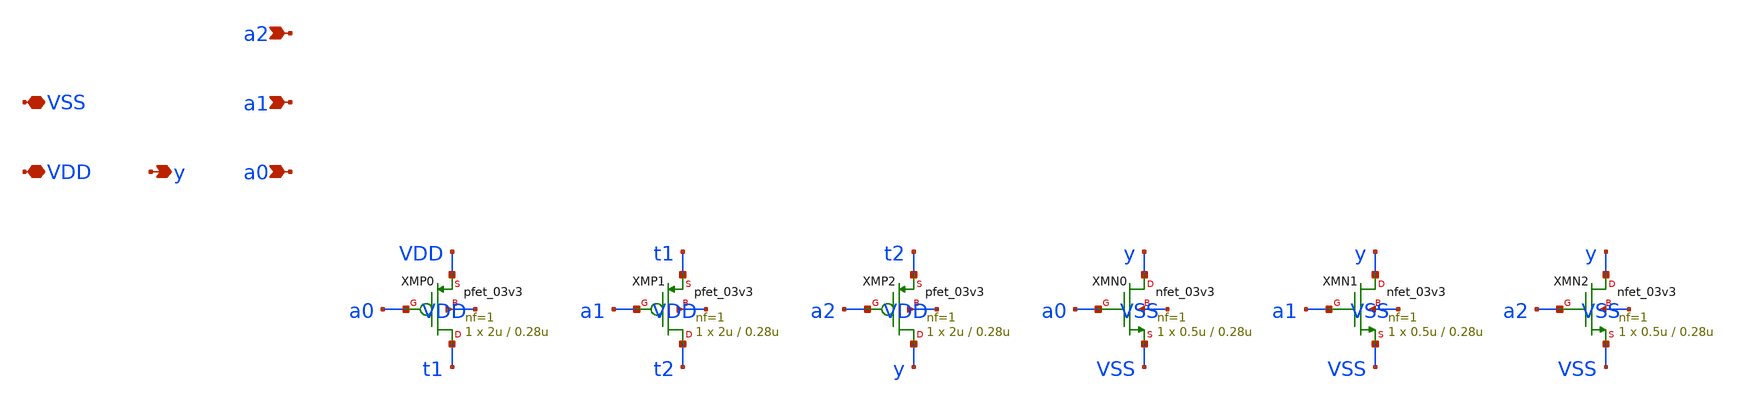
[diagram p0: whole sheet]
** sch_path: design/nor3.sch
**.subckt nor3 a0 a1 a2 y VDD VSS
*.ipin a0
*.ipin a1
*.ipin a2
*.opin y
*.iopin VDD
*.iopin VSS
XMP0 t1 a0 VDD VDD pfet_03v3 L=0.28u W=2u nf=1 ad='int((nf+1)/2) * W/nf * 0.18u' as='int((nf+2)/2) * W/nf * 0.18u'
+ pd='2*int((nf+1)/2) * (W/nf + 0.18u)' ps='2*int((nf+2)/2) * (W/nf + 0.18u)' nrd='0.18u / W' nrs='0.18u / W'
+ sa=0 sb=0 sd=0 m=1
XMP1 t2 a1 t1 VDD pfet_03v3 L=0.28u W=2u nf=1 ad='int((nf+1)/2) * W/nf * 0.18u' as='int((nf+2)/2) * W/nf * 0.18u'
+ pd='2*int((nf+1)/2) * (W/nf + 0.18u)' ps='2*int((nf+2)/2) * (W/nf + 0.18u)' nrd='0.18u / W' nrs='0.18u / W'
+ sa=0 sb=0 sd=0 m=1
XMP2 y a2 t2 VDD pfet_03v3 L=0.28u W=2u nf=1 ad='int((nf+1)/2) * W/nf * 0.18u' as='int((nf+2)/2) * W/nf * 0.18u'
+ pd='2*int((nf+1)/2) * (W/nf + 0.18u)' ps='2*int((nf+2)/2) * (W/nf + 0.18u)' nrd='0.18u / W' nrs='0.18u / W'
+ sa=0 sb=0 sd=0 m=1
XMN0 y a0 VSS VSS nfet_03v3 L=0.28u W=0.5u nf=1 ad='int((nf+1)/2) * W/nf * 0.18u' as='int((nf+2)/2) * W/nf * 0.18u'
+ pd='2*int((nf+1)/2) * (W/nf + 0.18u)' ps='2*int((nf+2)/2) * (W/nf + 0.18u)' nrd='0.18u / W' nrs='0.18u / W'
+ sa=0 sb=0 sd=0 m=1
XMN1 y a1 VSS VSS nfet_03v3 L=0.28u W=0.5u nf=1 ad='int((nf+1)/2) * W/nf * 0.18u' as='int((nf+2)/2) * W/nf * 0.18u'
+ pd='2*int((nf+1)/2) * (W/nf + 0.18u)' ps='2*int((nf+2)/2) * (W/nf + 0.18u)' nrd='0.18u / W' nrs='0.18u / W'
+ sa=0 sb=0 sd=0 m=1
XMN2 y a2 VSS VSS nfet_03v3 L=0.28u W=0.5u nf=1 ad='int((nf+1)/2) * W/nf * 0.18u' as='int((nf+2)/2) * W/nf * 0.18u'
+ pd='2*int((nf+1)/2) * (W/nf + 0.18u)' ps='2*int((nf+2)/2) * (W/nf + 0.18u)' nrd='0.18u / W' nrs='0.18u / W'
+ sa=0 sb=0 sd=0 m=1
**.ends
.end
